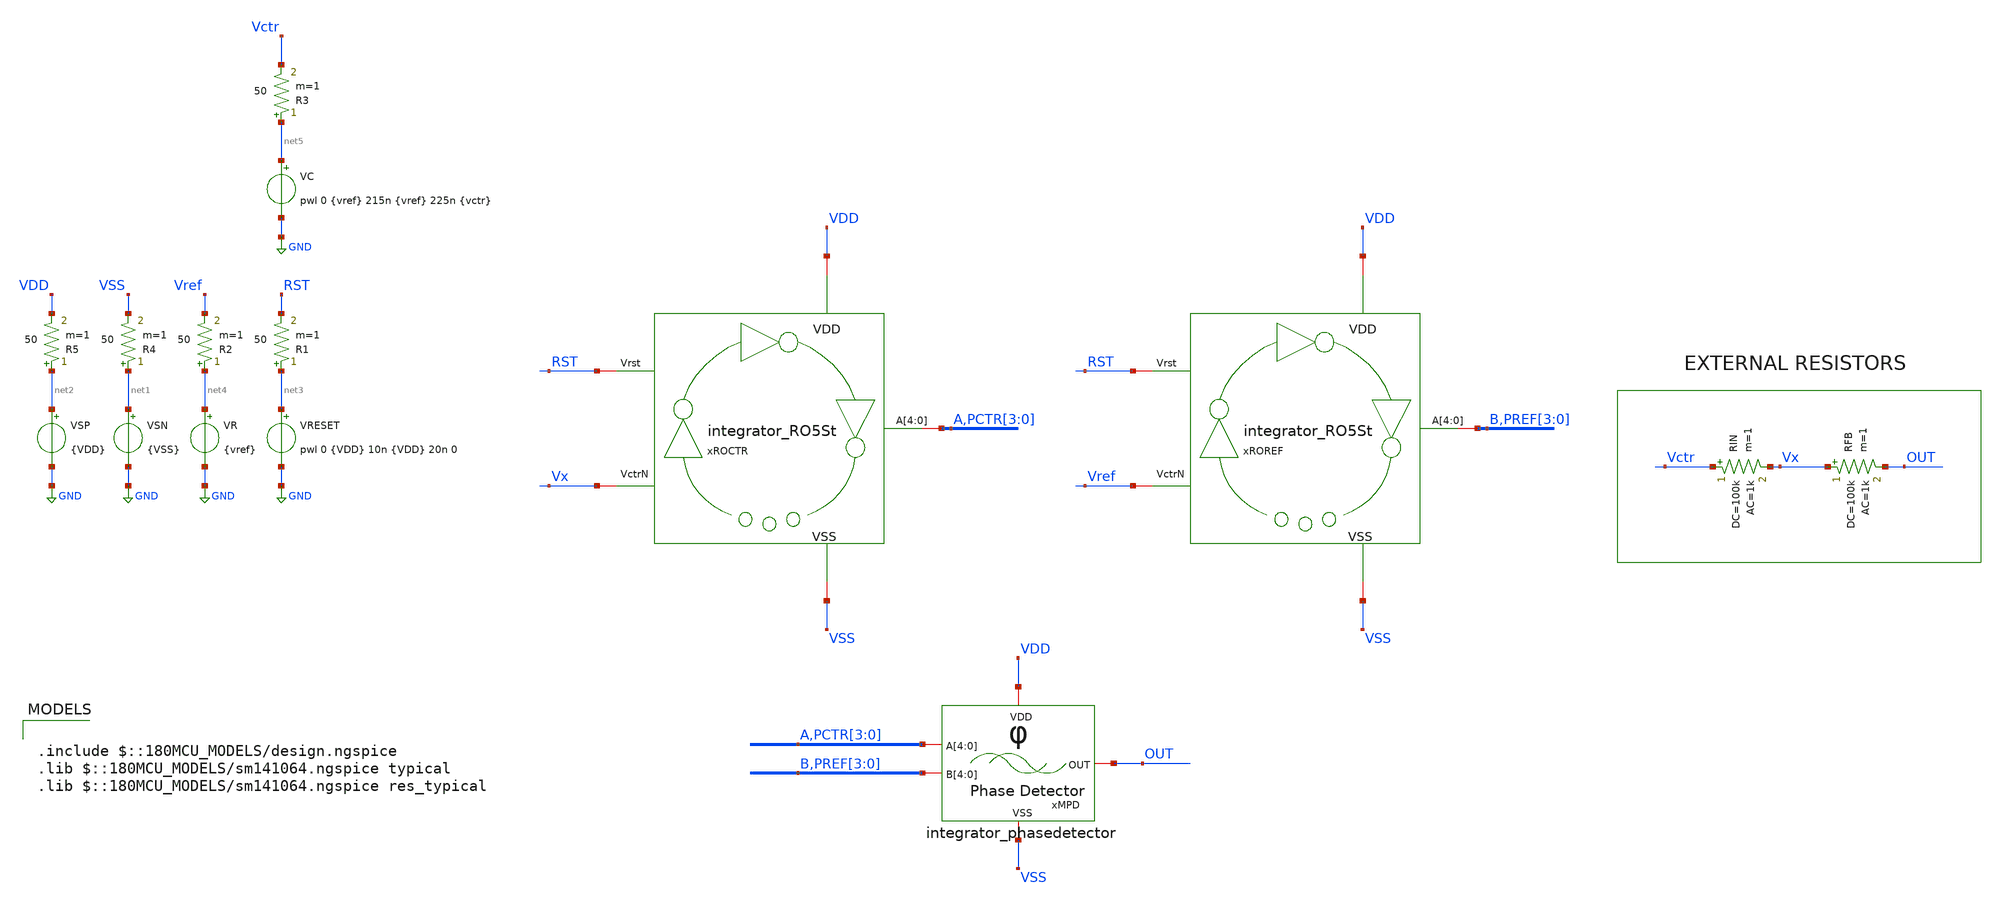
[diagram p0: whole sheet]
** sch_path: designs/ring_oscillator_pg/integrator/xschem/integrator&Resistors_TB.sch
**.subckt integrator&Resistors_TB
xROCTR VDD VSS Vx RST A PCTR[3] PCTR[2] PCTR[1] PCTR[0] integrator_RO5St
xROREF VDD VSS Vref RST B PREF[3] PREF[2] PREF[1] PREF[0] integrator_RO5St
xMPD VDD VSS A PCTR[3] PCTR[2] PCTR[1] PCTR[0] B PREF[3] PREF[2] PREF[1] PREF[0] OUT
+ integrator_phasedetector
VRESET net3 GND pwl 0 {VDD} 10n {VDD} 20n 0
VSP net2 GND {VDD}
VSN net1 GND {VSS}
VR net4 GND {vref}
VC net5 GND pwl 0 {vref} 215n {vref} 225n {vctr}
RIN Vctr Vx 100k ac=1k m=1
RFB Vx OUT 100k ac=1k m=1
R3 net5 Vctr 50 m=1
R1 net3 RST 50 m=1
R2 net4 Vref 50 m=1
R4 net1 VSS 50 m=1
R5 net2 VDD 50 m=1
**** begin user architecture code

.include $::180MCU_MODELS/design.ngspice
.lib $::180MCU_MODELS/sm141064.ngspice typical
.lib $::180MCU_MODELS/sm141064.ngspice res_typical





.param VDD = 1.8
.param VSS = 0
.param vctr = 1
.param vref = 1.3
.param cap = 15f

.param wxor=5.6u

.save all

.control

*----------------------------- Parámetros generales
let Vhigh = 1.8
let Vmid = Vhigh * 0.5

tran 0.1n 1u
meas tran IDD_AVG AVG i(VSP) from=20n to=1u
let PAVG = abs(IDD_AVG*Vhigh)
print PAVG

meas TRAN T_period TRIG v(B) VAL=Vmid rise=2 TARG v(B) VAL=Vmid rise=3
let F_ring = 1 / T_period
print F_ring

plot v(Vctr) v(Vref)
plot v(OUT) v(Vx)
plot v(RST)

.endc


**** end user architecture code
**.ends
.GLOBAL GND
.end
